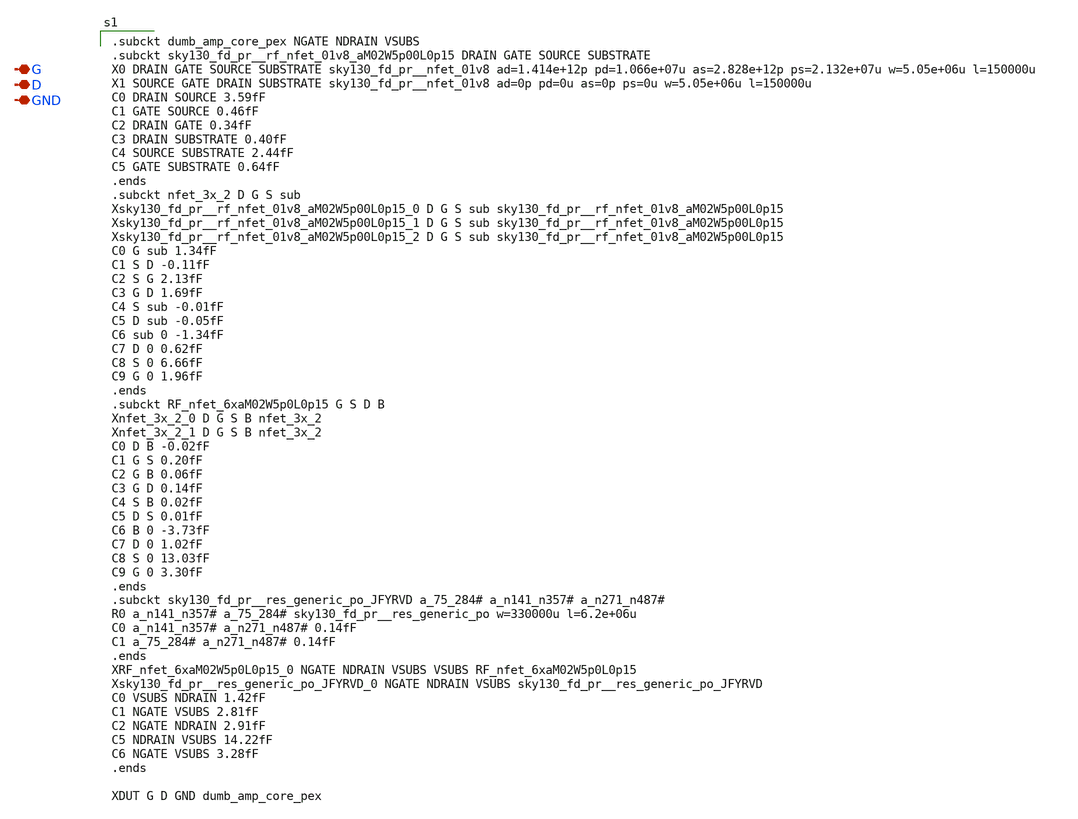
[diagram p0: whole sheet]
** sch_path: xschem/dumb_amp_r1_2_core_PEX.sch
**.subckt dumb_amp_r1_2_core_PEX G D GND
*.iopin G
*.iopin D
*.iopin GND
**** begin user architecture code

.subckt dumb_amp_core_pex NGATE NDRAIN VSUBS
.subckt sky130_fd_pr__rf_nfet_01v8_aM02W5p00L0p15 DRAIN GATE SOURCE SUBSTRATE
X0 DRAIN GATE SOURCE SUBSTRATE sky130_fd_pr__nfet_01v8 ad=1.414e+12p pd=1.066e+07u as=2.828e+12p
+ ps=2.132e+07u w=5.05e+06u l=150000u
X1 SOURCE GATE DRAIN SUBSTRATE sky130_fd_pr__nfet_01v8 ad=0p pd=0u as=0p ps=0u w=5.05e+06u l=150000u
C0 DRAIN SOURCE 3.59fF
C1 GATE SOURCE 0.46fF
C2 DRAIN GATE 0.34fF
C3 DRAIN SUBSTRATE 0.40fF
C4 SOURCE SUBSTRATE 2.44fF
C5 GATE SUBSTRATE 0.64fF
.ends
.subckt nfet_3x_2 D G S sub
Xsky130_fd_pr__rf_nfet_01v8_aM02W5p00L0p15_0 D G S sub sky130_fd_pr__rf_nfet_01v8_aM02W5p00L0p15
Xsky130_fd_pr__rf_nfet_01v8_aM02W5p00L0p15_1 D G S sub sky130_fd_pr__rf_nfet_01v8_aM02W5p00L0p15
Xsky130_fd_pr__rf_nfet_01v8_aM02W5p00L0p15_2 D G S sub sky130_fd_pr__rf_nfet_01v8_aM02W5p00L0p15
C0 G sub 1.34fF
C1 S D -0.11fF
C2 S G 2.13fF
C3 G D 1.69fF
C4 S sub -0.01fF
C5 D sub -0.05fF
C6 sub 0 -1.34fF
C7 D 0 0.62fF
C8 S 0 6.66fF
C9 G 0 1.96fF
.ends
.subckt RF_nfet_6xaM02W5p0L0p15 G S D B
Xnfet_3x_2_0 D G S B nfet_3x_2
Xnfet_3x_2_1 D G S B nfet_3x_2
C0 D B -0.02fF
C1 G S 0.20fF
C2 G B 0.06fF
C3 G D 0.14fF
C4 S B 0.02fF
C5 D S 0.01fF
C6 B 0 -3.73fF
C7 D 0 1.02fF
C8 S 0 13.03fF
C9 G 0 3.30fF
.ends
.subckt sky130_fd_pr__res_generic_po_JFYRVD a_75_284# a_n141_n357# a_n271_n487#
R0 a_n141_n357# a_75_284# sky130_fd_pr__res_generic_po w=330000u l=6.2e+06u
C0 a_n141_n357# a_n271_n487# 0.14fF
C1 a_75_284# a_n271_n487# 0.14fF
.ends
XRF_nfet_6xaM02W5p0L0p15_0 NGATE NDRAIN VSUBS VSUBS RF_nfet_6xaM02W5p0L0p15
Xsky130_fd_pr__res_generic_po_JFYRVD_0 NGATE NDRAIN VSUBS sky130_fd_pr__res_generic_po_JFYRVD
C0 VSUBS NDRAIN 1.42fF
C1 NGATE VSUBS 2.81fF
C2 NGATE NDRAIN 2.91fF
C5 NDRAIN VSUBS 14.22fF
C6 NGATE VSUBS 3.28fF
.ends

XDUT G D GND dumb_amp_core_pex


**** end user architecture code
**.ends
.end
